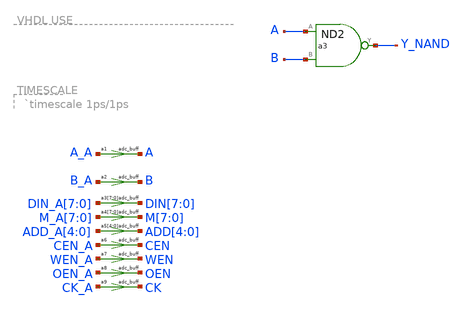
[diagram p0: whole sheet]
** sch_path: xschem_library/logic/test_ngspice.sch
**.subckt test_ngspice
a1 [ A_A ] [ A ] adc_buff
a2 [ B_A ] [ B ] adc_buff
a3[7] [ DIN_A[7] ] [ DIN[7] ] adc_buff
a3[6] [ DIN_A[6] ] [ DIN[6] ] adc_buff
a3[5] [ DIN_A[5] ] [ DIN[5] ] adc_buff
a3[4] [ DIN_A[4] ] [ DIN[4] ] adc_buff
a3[3] [ DIN_A[3] ] [ DIN[3] ] adc_buff
a3[2] [ DIN_A[2] ] [ DIN[2] ] adc_buff
a3[1] [ DIN_A[1] ] [ DIN[1] ] adc_buff
a3[0] [ DIN_A[0] ] [ DIN[0] ] adc_buff
a4[7] [ M_A[7] ] [ M[7] ] adc_buff
a4[6] [ M_A[6] ] [ M[6] ] adc_buff
a4[5] [ M_A[5] ] [ M[5] ] adc_buff
a4[4] [ M_A[4] ] [ M[4] ] adc_buff
a4[3] [ M_A[3] ] [ M[3] ] adc_buff
a4[2] [ M_A[2] ] [ M[2] ] adc_buff
a4[1] [ M_A[1] ] [ M[1] ] adc_buff
a4[0] [ M_A[0] ] [ M[0] ] adc_buff
a5[4] [ ADD_A[4] ] [ ADD[4] ] adc_buff
a5[3] [ ADD_A[3] ] [ ADD[3] ] adc_buff
a5[2] [ ADD_A[2] ] [ ADD[2] ] adc_buff
a5[1] [ ADD_A[1] ] [ ADD[1] ] adc_buff
a5[0] [ ADD_A[0] ] [ ADD[0] ] adc_buff
a6 [ CEN_A ] [ CEN ] adc_buff
a7 [ WEN_A ] [ WEN ] adc_buff
a8 [ OEN_A ] [ OEN ] adc_buff
a9 [ CK_A ] [ CK ] adc_buff
a3 [ A B ] Y_NAND nand
**** begin user architecture code
.model adc_buff adc_bridge(in_low = 0.3 in_high = 0.7)


.model nand d_nand(rise_delay = 0.5e-9 fall_delay = 0.3e-9  input_load = 5e-15)
**** end user architecture code
**.ends

* expanding   symbol:  nd2.sym # of pins=3
** sym_path: xschem_library/logic/nd2.sym
** sch_path: xschem_library/logic/nd2.sch
.subckt nd2 A B Y  delay=120 ps del=120
.ends

**** begin user architecture code



.include stimuli.cir

.control
tran 100n 26u
eprvcd A B Y_NAND  > zzzz.vcd
.endc


**** end user architecture code
.end
